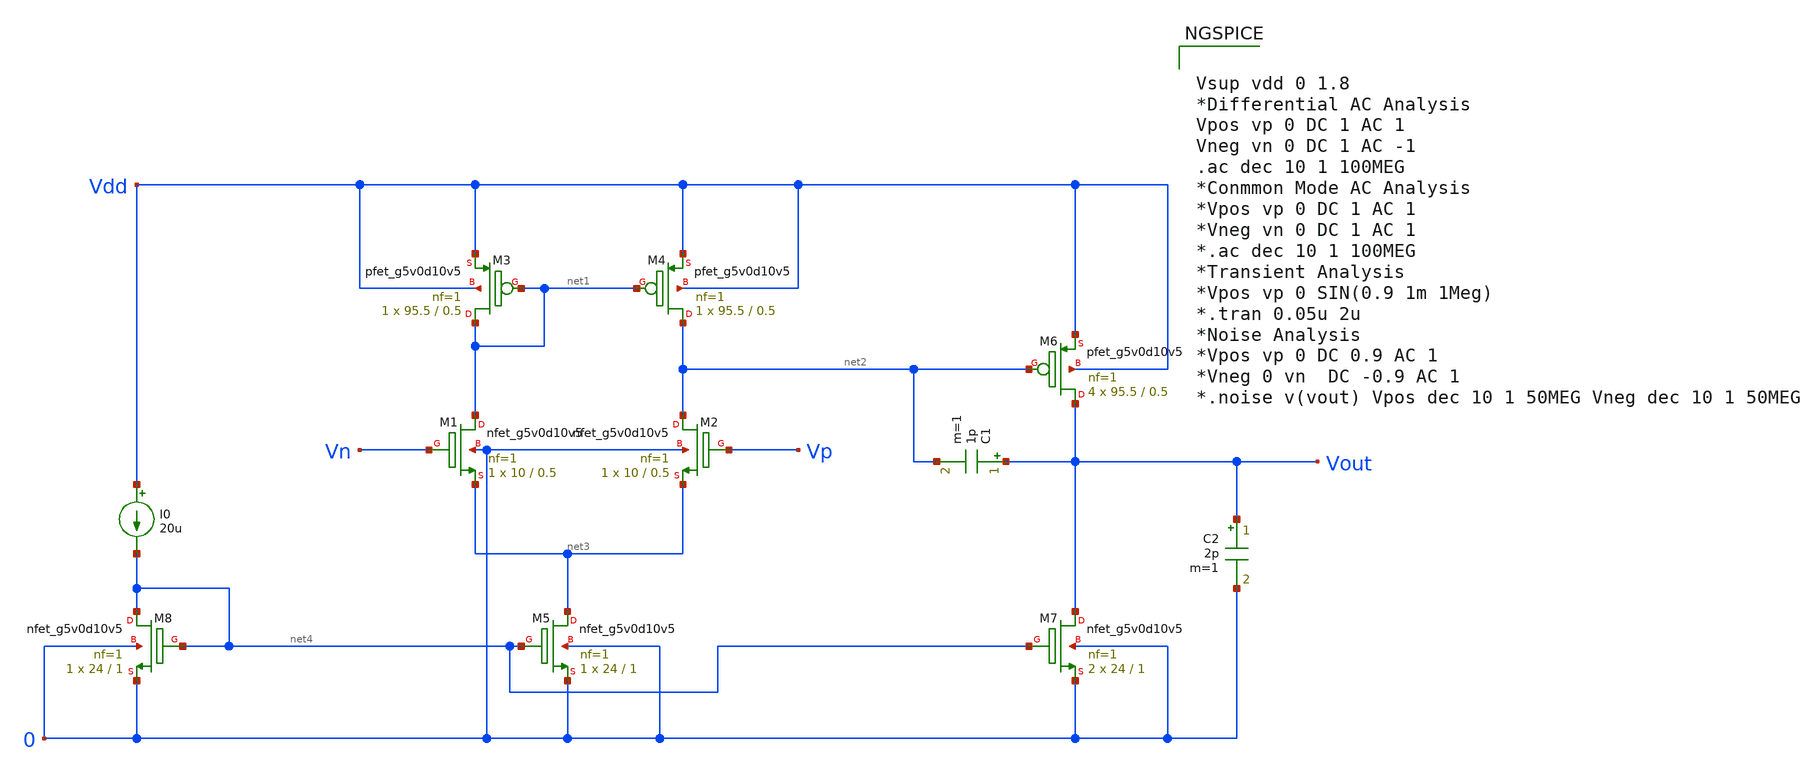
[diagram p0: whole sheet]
** sch_path: OTA/Schematic/Miller_OTA_NMOS.sch
**.subckt Miller_OTA_NMOS
C1 Vout net2 1p m=1
I0 Vdd net4 20u
XM1 net1 Vn net3 0 sky130_fd_pr__nfet_g5v0d10v5 L=0.5 W=10 nf=1 ad='int((nf+1)/2) * W/nf * 0.29' as='int((nf+2)/2) * W/nf * 0.29'
+ pd='2*int((nf+1)/2) * (W/nf + 0.29)' ps='2*int((nf+2)/2) * (W/nf + 0.29)' nrd='0.29 / W' nrs='0.29 / W'
+ sa=0 sb=0 sd=0 mult=1 m=1
XM2 net2 Vp net3 0 sky130_fd_pr__nfet_g5v0d10v5 L=0.5 W=10 nf=1 ad='int((nf+1)/2) * W/nf * 0.29' as='int((nf+2)/2) * W/nf * 0.29'
+ pd='2*int((nf+1)/2) * (W/nf + 0.29)' ps='2*int((nf+2)/2) * (W/nf + 0.29)' nrd='0.29 / W' nrs='0.29 / W'
+ sa=0 sb=0 sd=0 mult=1 m=1
XM3 net1 net1 Vdd Vdd sky130_fd_pr__pfet_g5v0d10v5 L=0.5 W=95.5 nf=1 ad='int((nf+1)/2) * W/nf * 0.29'
+ as='int((nf+2)/2) * W/nf * 0.29' pd='2*int((nf+1)/2) * (W/nf + 0.29)' ps='2*int((nf+2)/2) * (W/nf + 0.29)'
+ nrd='0.29 / W' nrs='0.29 / W' sa=0 sb=0 sd=0 mult=1 m=1
XM4 net2 net1 Vdd Vdd sky130_fd_pr__pfet_g5v0d10v5 L=0.5 W=95.5 nf=1 ad='int((nf+1)/2) * W/nf * 0.29'
+ as='int((nf+2)/2) * W/nf * 0.29' pd='2*int((nf+1)/2) * (W/nf + 0.29)' ps='2*int((nf+2)/2) * (W/nf + 0.29)'
+ nrd='0.29 / W' nrs='0.29 / W' sa=0 sb=0 sd=0 mult=1 m=1
XM6 Vout net2 Vdd Vdd sky130_fd_pr__pfet_g5v0d10v5 L=0.5 W=95.5 nf=1 ad='int((nf+1)/2) * W/nf * 0.29'
+ as='int((nf+2)/2) * W/nf * 0.29' pd='2*int((nf+1)/2) * (W/nf + 0.29)' ps='2*int((nf+2)/2) * (W/nf + 0.29)'
+ nrd='0.29 / W' nrs='0.29 / W' sa=0 sb=0 sd=0 mult=4 m=4
XM5 net3 net4 0 0 sky130_fd_pr__nfet_g5v0d10v5 L=1 W=24 nf=1 ad='int((nf+1)/2) * W/nf * 0.29' as='int((nf+2)/2) * W/nf * 0.29'
+ pd='2*int((nf+1)/2) * (W/nf + 0.29)' ps='2*int((nf+2)/2) * (W/nf + 0.29)' nrd='0.29 / W' nrs='0.29 / W'
+ sa=0 sb=0 sd=0 mult=1 m=1
XM8 net4 net4 0 0 sky130_fd_pr__nfet_g5v0d10v5 L=1 W=24 nf=1 ad='int((nf+1)/2) * W/nf * 0.29' as='int((nf+2)/2) * W/nf * 0.29'
+ pd='2*int((nf+1)/2) * (W/nf + 0.29)' ps='2*int((nf+2)/2) * (W/nf + 0.29)' nrd='0.29 / W' nrs='0.29 / W'
+ sa=0 sb=0 sd=0 mult=1 m=1
XM7 Vout net4 0 0 sky130_fd_pr__nfet_g5v0d10v5 L=1 W=24 nf=1 ad='int((nf+1)/2) * W/nf * 0.29' as='int((nf+2)/2) * W/nf * 0.29'
+ pd='2*int((nf+1)/2) * (W/nf + 0.29)' ps='2*int((nf+2)/2) * (W/nf + 0.29)' nrd='0.29 / W' nrs='0.29 / W'
+ sa=0 sb=0 sd=0 mult=2 m=2
C2 Vout 0 2p m=1
**** begin user architecture code

.include $::SKYWATER_MODELS/cells/nfet_01v8/sky130_fd_pr__nfet_01v8__tt.corner.spice
.include $::SKYWATER_MODELS/cells/nfet_01v8_lvt/sky130_fd_pr__nfet_01v8_lvt__tt.corner.spice
.include $::SKYWATER_MODELS/cells/pfet_01v8/sky130_fd_pr__pfet_01v8__tt.corner.spice
.include $::SKYWATER_MODELS/cells/nfet_03v3_nvt/sky130_fd_pr__nfet_03v3_nvt__tt.corner.spice
.include $::SKYWATER_MODELS/cells/nfet_05v0_nvt/sky130_fd_pr__nfet_05v0_nvt__tt.corner.spice
.include $::SKYWATER_MODELS/cells/esd_nfet_01v8/sky130_fd_pr__esd_nfet_01v8__tt.corner.spice
.include $::SKYWATER_MODELS/cells/pfet_01v8_lvt/sky130_fd_pr__pfet_01v8_lvt__tt.corner.spice
.include $::SKYWATER_MODELS/cells/pfet_01v8_hvt/sky130_fd_pr__pfet_01v8_hvt__tt.corner.spice
.include $::SKYWATER_MODELS/cells/esd_pfet_g5v0d10v5/sky130_fd_pr__esd_pfet_g5v0d10v5__tt.corner.spice
.include $::SKYWATER_MODELS/cells/pfet_g5v0d10v5/sky130_fd_pr__pfet_g5v0d10v5__tt.corner.spice
.include $::SKYWATER_MODELS/cells/pfet_g5v0d16v0/sky130_fd_pr__pfet_g5v0d16v0__tt.corner.spice
.include $::SKYWATER_MODELS/cells/nfet_g5v0d10v5/sky130_fd_pr__nfet_g5v0d10v5__tt.corner.spice
.include $::SKYWATER_MODELS/cells/nfet_g5v0d16v0/sky130_fd_pr__nfet_g5v0d16v0__tt_discrete.corner.spice
.include $::SKYWATER_MODELS/cells/esd_nfet_g5v0d10v5/sky130_fd_pr__esd_nfet_g5v0d10v5__tt.corner.spice
.include $::SKYWATER_MODELS/models/corners/tt/nonfet.spice
* Mismatch parameters
.include $::SKYWATER_MODELS/cells/nfet_01v8/sky130_fd_pr__nfet_01v8__mismatch.corner.spice
.include $::SKYWATER_MODELS/cells/pfet_01v8/sky130_fd_pr__pfet_01v8__mismatch.corner.spice
.include $::SKYWATER_MODELS/cells/nfet_01v8_lvt/sky130_fd_pr__nfet_01v8_lvt__mismatch.corner.spice
.include $::SKYWATER_MODELS/cells/pfet_01v8_lvt/sky130_fd_pr__pfet_01v8_lvt__mismatch.corner.spice
.include $::SKYWATER_MODELS/cells/pfet_01v8_hvt/sky130_fd_pr__pfet_01v8_hvt__mismatch.corner.spice
.include $::SKYWATER_MODELS/cells/nfet_g5v0d10v5/sky130_fd_pr__nfet_g5v0d10v5__mismatch.corner.spice
.include $::SKYWATER_MODELS/cells/pfet_g5v0d10v5/sky130_fd_pr__pfet_g5v0d10v5__mismatch.corner.spice
.include $::SKYWATER_MODELS/cells/nfet_05v0_nvt/sky130_fd_pr__nfet_05v0_nvt__mismatch.corner.spice
.include $::SKYWATER_MODELS/cells/nfet_03v3_nvt/sky130_fd_pr__nfet_03v3_nvt__mismatch.corner.spice
* Resistor$::SKYWATER_MODELS/Capacitor
.include $::SKYWATER_MODELS/models/r+c/res_typical__cap_typical.spice
.include $::SKYWATER_MODELS/models/r+c/res_typical__cap_typical__lin.spice
* Special cells
.include $::SKYWATER_MODELS/models/corners/tt/specialized_cells.spice
* All models
.include $::SKYWATER_MODELS/models/all.spice
* Corner
.include $::SKYWATER_MODELS/models/corners/tt/rf.spice



Vsup vdd 0 1.8
*Differential AC Analysis
Vpos vp 0 DC 1 AC 1
Vneg vn 0 DC 1 AC -1
.ac dec 10 1 100MEG
*Conmmon Mode AC Analysis
*Vpos vp 0 DC 1 AC 1
*Vneg vn 0 DC 1 AC 1
*.ac dec 10 1 100MEG
*Transient Analysis
*Vpos vp 0 SIN(0.9 1m 1Meg)
*.tran 0.05u 2u
*Noise Analysis
*Vpos vp 0 DC 0.9 AC 1
*Vneg 0 vn  DC -0.9 AC 1
*.noise v(vout) Vpos dec 10 1 50MEG Vneg dec 10 1 50MEG


**** end user architecture code
**.ends
.end
